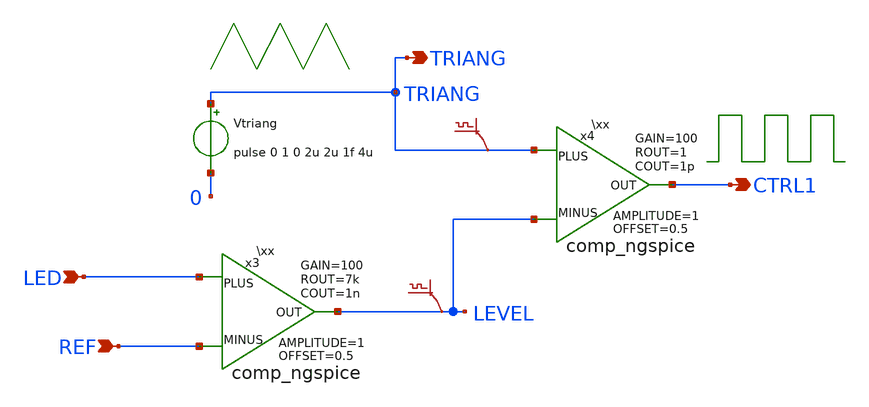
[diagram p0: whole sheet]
** sch_path: xschem_libraries_oa/SANDBOX/solar_ctl/schematic/solar_ctl.sch
* StefanSchippers/xschem/xschem_library/ngspice/comp_ngspice.sch:
* Copyright (C) 1998-2026 Stefan Frederik Schippers
* This program is free software; you can redistribute it and/or modify
* it under the terms of the GNU General Public License as published by
* the Free Software Foundation; either version 2 of the License, or
* (at your option) any later version.
**.subckt solar_ctl LED REF CTRL1 TRIANG
*.ipin LED
*.ipin REF
*.opin CTRL1
*.opin TRIANG
Vtriang TRIANG 0 pulse 0 1 0 2u 2u 1f 4u
x3 LED LEVEL REF comp_ngspice OFFSET=0.5 AMPLITUDE=1 GAIN=100 ROUT=7k COUT=1n
x4 TRIANG CTRL1 LEVEL comp_ngspice OFFSET=0.5 AMPLITUDE=1 GAIN=100 ROUT=1 COUT=1p
.save v(triang)
.save v(level)
**.ends

* expanding   symbol:  ngspice/comp_ngspice.sym # of pins=3
** sym_path: ngspice/comp_ngspice.sym
** sch_path: ngspice/comp_ngspice.sch
.subckt comp_ngspice PLUS OUT MINUS  OFFSET=0 AMPLITUDE=5 GAIN=100 ROUT=1000 COUT=1p
*.ipin PLUS
*.ipin MINUS
*.opin OUT
B1 IOUT 0 V = {OFFSET + AMPLITUDE/2*(tanh(V(IPLUS,IMINUS)*GAIN*2/AMPLITUDE))}
R1 OUT IOUT {ROUT} m=1
C3 OUT 0 {COUT} m=1
V1 IPLUS PLUS 0
V2 IMINUS MINUS 0
.ends

.end
